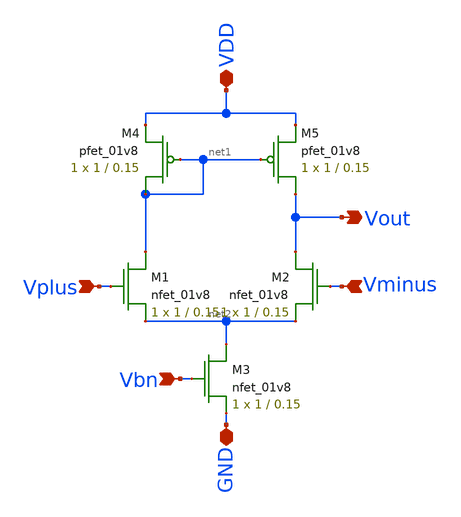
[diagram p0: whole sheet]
** sch_path: final/schematics/opamp.sch
**.subckt opamp VDD GND Vplus Vminus Vout Vbn
*.iopin VDD
*.iopin GND
*.ipin Vplus
*.ipin Vminus
*.opin Vout
*.ipin Vbn
XM1 net1 Vplus net2 GND sky130_fd_pr__nfet_01v8 L=0.15 W=1 nf=1 ad='int((nf+1)/2) * W/nf * 0.29' as='int((nf+2)/2) * W/nf * 0.29'
+ pd='2*int((nf+1)/2) * (W/nf + 0.29)' ps='2*int((nf+2)/2) * (W/nf + 0.29)' nrd='0.29 / W' nrs='0.29 / W'
+ sa=0 sb=0 sd=0 mult=1 m=1
XM2 Vout Vminus net2 GND sky130_fd_pr__nfet_01v8 L=0.15 W=1 nf=1 ad='int((nf+1)/2) * W/nf * 0.29' as='int((nf+2)/2) * W/nf * 0.29'
+ pd='2*int((nf+1)/2) * (W/nf + 0.29)' ps='2*int((nf+2)/2) * (W/nf + 0.29)' nrd='0.29 / W' nrs='0.29 / W'
+ sa=0 sb=0 sd=0 mult=1 m=1
XM3 net2 Vbn GND GND sky130_fd_pr__nfet_01v8 L=0.15 W=1 nf=1 ad='int((nf+1)/2) * W/nf * 0.29' as='int((nf+2)/2) * W/nf * 0.29'
+ pd='2*int((nf+1)/2) * (W/nf + 0.29)' ps='2*int((nf+2)/2) * (W/nf + 0.29)' nrd='0.29 / W' nrs='0.29 / W'
+ sa=0 sb=0 sd=0 mult=1 m=1
XM4 net1 net1 VDD VDD sky130_fd_pr__pfet_01v8 L=0.15 W=1 nf=1 ad='int((nf+1)/2) * W/nf * 0.29' as='int((nf+2)/2) * W/nf * 0.29'
+ pd='2*int((nf+1)/2) * (W/nf + 0.29)' ps='2*int((nf+2)/2) * (W/nf + 0.29)' nrd='0.29 / W' nrs='0.29 / W'
+ sa=0 sb=0 sd=0 mult=1 m=1
XM5 Vout net1 VDD VDD sky130_fd_pr__pfet_01v8 L=0.15 W=1 nf=1 ad='int((nf+1)/2) * W/nf * 0.29' as='int((nf+2)/2) * W/nf * 0.29'
+ pd='2*int((nf+1)/2) * (W/nf + 0.29)' ps='2*int((nf+2)/2) * (W/nf + 0.29)' nrd='0.29 / W' nrs='0.29 / W'
+ sa=0 sb=0 sd=0 mult=1 m=1
**.ends
.end
